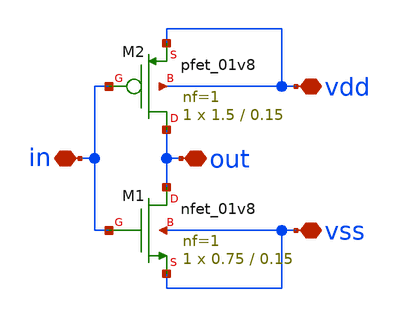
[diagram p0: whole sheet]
** sch_path: design/blocks/inverter/schematic/inverter.sch
**.subckt inverter vdd out vss in
*.iopin vdd
*.iopin out
*.iopin vss
*.iopin in
XM1 out in vss vss sky130_fd_pr__nfet_01v8 L=0.15 W=0.75 nf=1 ad='int((nf+1)/2) * W/nf * 0.29' as='int((nf+2)/2) * W/nf * 0.29'
+ pd='2*int((nf+1)/2) * (W/nf + 0.29)' ps='2*int((nf+2)/2) * (W/nf + 0.29)' nrd='0.29 / W' nrs='0.29 / W'
+ sa=0 sb=0 sd=0 mult=1 m=1
XM2 out in vdd vdd sky130_fd_pr__pfet_01v8 L=0.15 W=1.5 nf=1 ad='int((nf+1)/2) * W/nf * 0.29' as='int((nf+2)/2) * W/nf * 0.29'
+ pd='2*int((nf+1)/2) * (W/nf + 0.29)' ps='2*int((nf+2)/2) * (W/nf + 0.29)' nrd='0.29 / W' nrs='0.29 / W'
+ sa=0 sb=0 sd=0 mult=1 m=1
**.ends
.end
